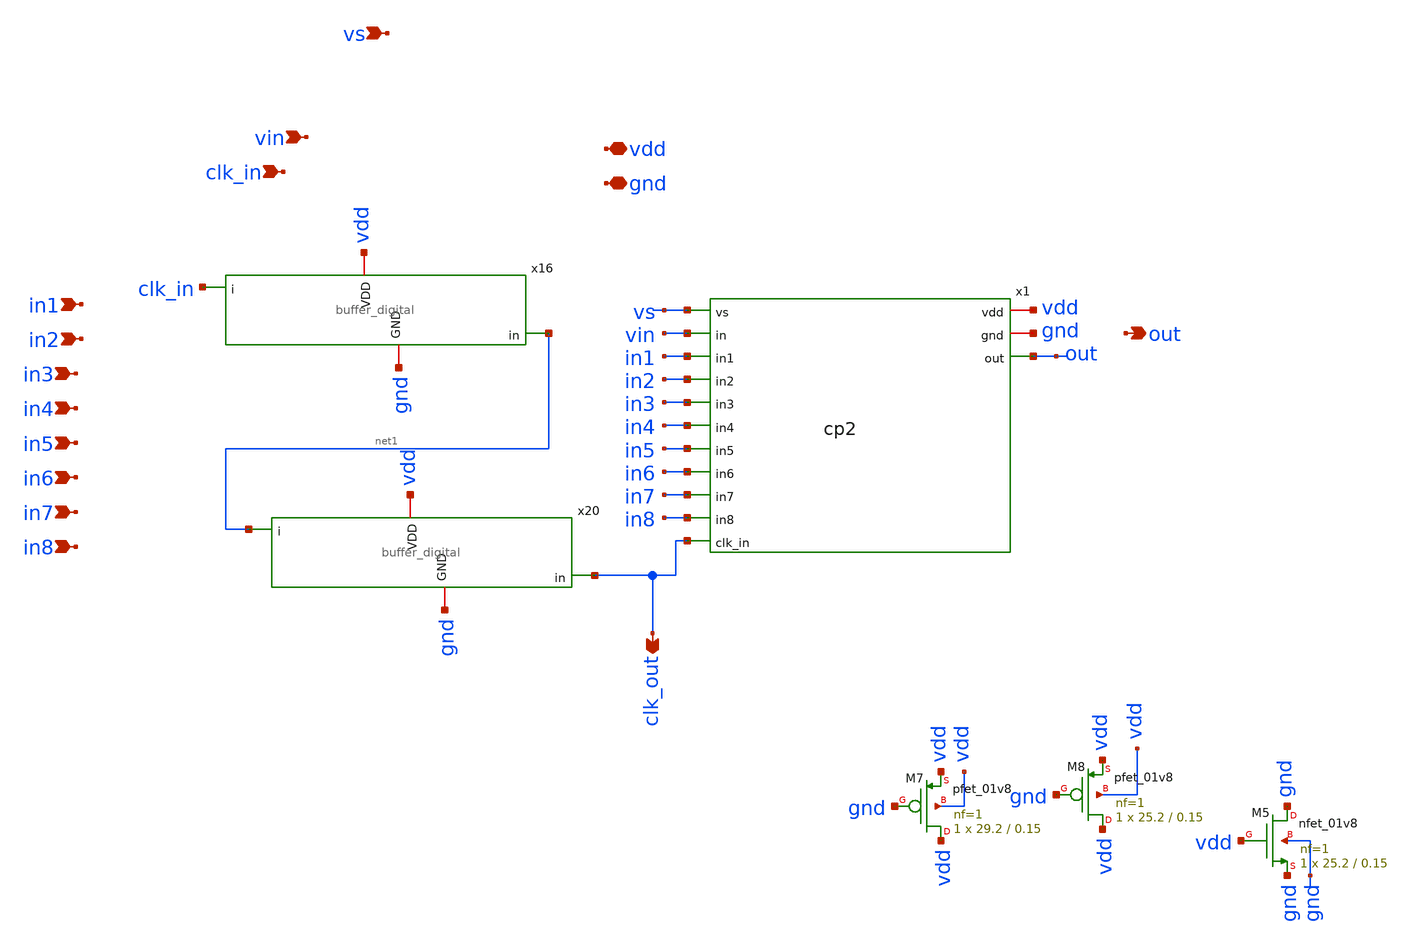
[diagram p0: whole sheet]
** sch_path: xschem/charge_pumps2/cp2_buffer.sch
**.subckt cp2_buffer gnd vdd vin out clk_in in1 in2 in3 in4 in5 in6 in7 in8 vs clk_out
*.iopin gnd
*.iopin vdd
*.ipin vin
*.opin out
*.ipin clk_in
*.ipin in1
*.ipin in2
*.ipin in3
*.ipin in4
*.ipin in5
*.ipin in6
*.ipin in7
*.ipin in8
*.ipin vs
*.opin clk_out
x16 gnd vdd clk_in net1 buffer_digital
x20 gnd vdd net1 clk_out buffer_digital
x1 vs vin vdd gnd in1 in2 in3 in4 in5 in6 in7 in8 clk_out out cp2
XM5 gnd vdd gnd gnd sky130_fd_pr__nfet_01v8 L=0.15 W=25.2 nf=1 ad='int((nf+1)/2) * W/nf * 0.29' as='int((nf+2)/2) * W/nf * 0.29'
+ pd='2*int((nf+1)/2) * (W/nf + 0.29)' ps='2*int((nf+2)/2) * (W/nf + 0.29)' nrd='0.29 / W' nrs='0.29 / W'
+ sa=0 sb=0 sd=0 mult=1 m=1
XM7 vdd gnd vdd vdd sky130_fd_pr__pfet_01v8 L=0.15 W=29.2 nf=1 ad='int((nf+1)/2) * W/nf * 0.29' as='int((nf+2)/2) * W/nf * 0.29'
+ pd='2*int((nf+1)/2) * (W/nf + 0.29)' ps='2*int((nf+2)/2) * (W/nf + 0.29)' nrd='0.29 / W' nrs='0.29 / W'
+ sa=0 sb=0 sd=0 mult=1 m=1
XM8 vdd gnd vdd vdd sky130_fd_pr__pfet_01v8 L=0.15 W=25.2 nf=1 ad='int((nf+1)/2) * W/nf * 0.29' as='int((nf+2)/2) * W/nf * 0.29'
+ pd='2*int((nf+1)/2) * (W/nf + 0.29)' ps='2*int((nf+2)/2) * (W/nf + 0.29)' nrd='0.29 / W' nrs='0.29 / W'
+ sa=0 sb=0 sd=0 mult=1 m=1
**.ends
.end
